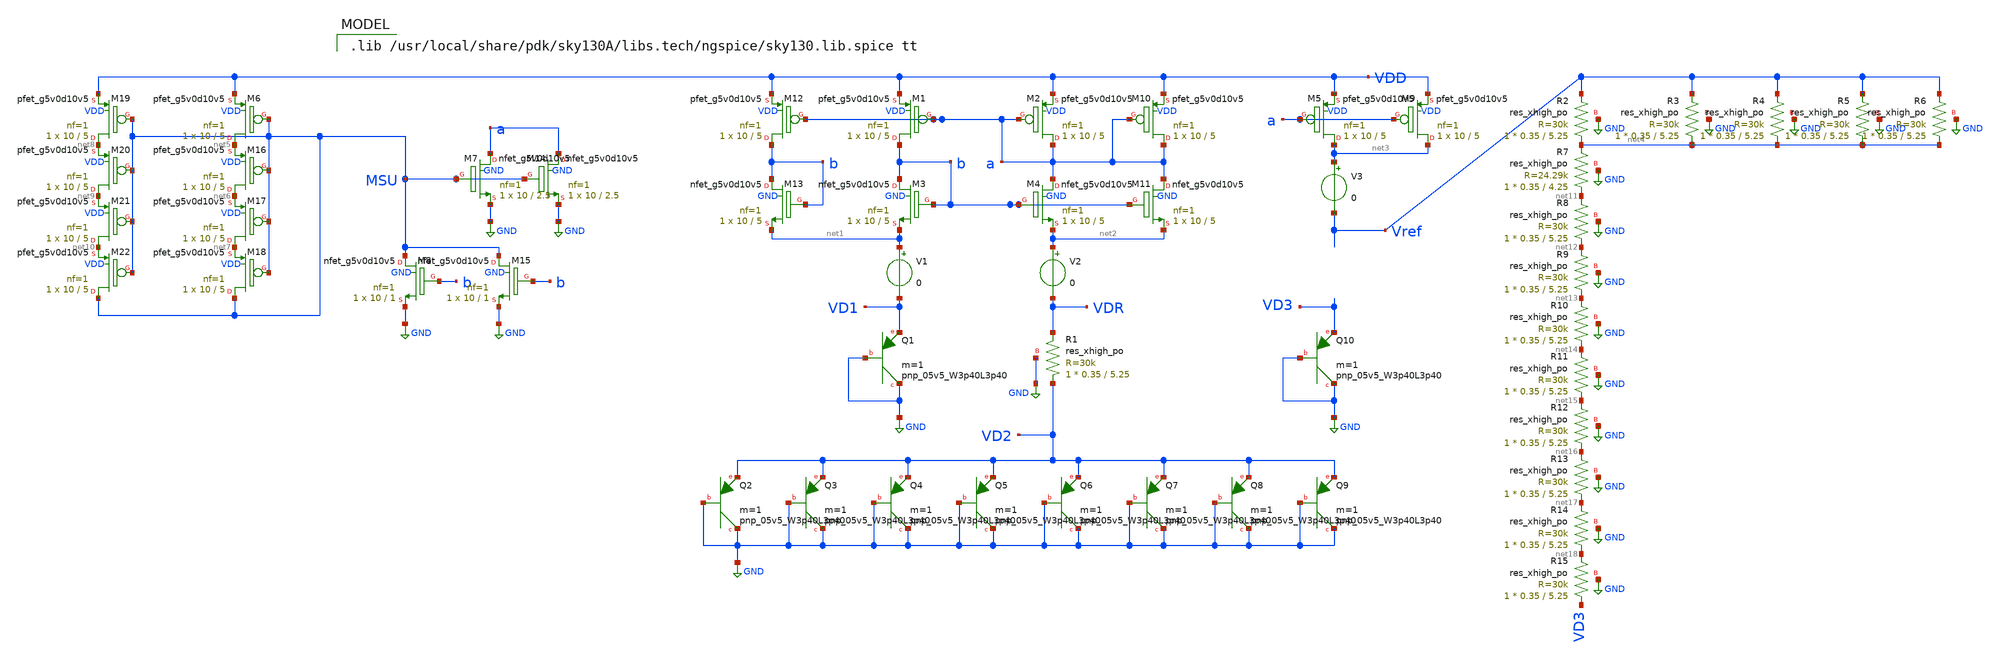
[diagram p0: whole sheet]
** sch_path: 2_BGR_nocas_30k_3p4pnp_finger.sch
**.subckt 2_BGR_nocas_30k_3p4pnp_finger
V1 net1 VD1 0
V2 net2 VDR 0
V3 net3 Vref 0
XM1 b a VDD VDD sky130_fd_pr__pfet_g5v0d10v5 L=5 W=10 nf=1 ad='int((nf+1)/2) * W/nf * 0.29' as='int((nf+2)/2) * W/nf * 0.29'
+ pd='2*int((nf+1)/2) * (W/nf + 0.29)' ps='2*int((nf+2)/2) * (W/nf + 0.29)' nrd='0.29 / W' nrs='0.29 / W'
+ sa=0 sb=0 sd=0 mult=1 m=1
XM2 a a VDD VDD sky130_fd_pr__pfet_g5v0d10v5 L=5 W=10 nf=1 ad='int((nf+1)/2) * W/nf * 0.29' as='int((nf+2)/2) * W/nf * 0.29'
+ pd='2*int((nf+1)/2) * (W/nf + 0.29)' ps='2*int((nf+2)/2) * (W/nf + 0.29)' nrd='0.29 / W' nrs='0.29 / W'
+ sa=0 sb=0 sd=0 mult=1 m=1
XM3 b b net1 GND sky130_fd_pr__nfet_g5v0d10v5 L=5 W=10 nf=1 ad='int((nf+1)/2) * W/nf * 0.29' as='int((nf+2)/2) * W/nf * 0.29'
+ pd='2*int((nf+1)/2) * (W/nf + 0.29)' ps='2*int((nf+2)/2) * (W/nf + 0.29)' nrd='0.29 / W' nrs='0.29 / W'
+ sa=0 sb=0 sd=0 mult=1 m=1
XM4 a b net2 GND sky130_fd_pr__nfet_g5v0d10v5 L=5 W=10 nf=1 ad='int((nf+1)/2) * W/nf * 0.29' as='int((nf+2)/2) * W/nf * 0.29'
+ pd='2*int((nf+1)/2) * (W/nf + 0.29)' ps='2*int((nf+2)/2) * (W/nf + 0.29)' nrd='0.29 / W' nrs='0.29 / W'
+ sa=0 sb=0 sd=0 mult=1 m=1
XM5 net3 a VDD VDD sky130_fd_pr__pfet_g5v0d10v5 L=5 W=10 nf=1 ad='int((nf+1)/2) * W/nf * 0.29' as='int((nf+2)/2) * W/nf * 0.29'
+ pd='2*int((nf+1)/2) * (W/nf + 0.29)' ps='2*int((nf+2)/2) * (W/nf + 0.29)' nrd='0.29 / W' nrs='0.29 / W'
+ sa=0 sb=0 sd=0 mult=1 m=1
XM8 MSU b GND GND sky130_fd_pr__nfet_g5v0d10v5 L=1 W=10 nf=1 ad='int((nf+1)/2) * W/nf * 0.29' as='int((nf+2)/2) * W/nf * 0.29'
+ pd='2*int((nf+1)/2) * (W/nf + 0.29)' ps='2*int((nf+2)/2) * (W/nf + 0.29)' nrd='0.29 / W' nrs='0.29 / W'
+ sa=0 sb=0 sd=0 mult=1 m=1
XM7 a MSU GND GND sky130_fd_pr__nfet_g5v0d10v5 L=2.5 W=10 nf=1 ad='int((nf+1)/2) * W/nf * 0.29' as='int((nf+2)/2) * W/nf * 0.29'
+ pd='2*int((nf+1)/2) * (W/nf + 0.29)' ps='2*int((nf+2)/2) * (W/nf + 0.29)' nrd='0.29 / W' nrs='0.29 / W'
+ sa=0 sb=0 sd=0 mult=1 m=1
XQ1 GND GND VD1 sky130_fd_pr__pnp_05v5_W3p40L3p40 m=1
XQ2 GND GND VD2 sky130_fd_pr__pnp_05v5_W3p40L3p40 m=1
XQ3 GND GND VD2 sky130_fd_pr__pnp_05v5_W3p40L3p40 m=1
XQ4 GND GND VD2 sky130_fd_pr__pnp_05v5_W3p40L3p40 m=1
XQ5 GND GND VD2 sky130_fd_pr__pnp_05v5_W3p40L3p40 m=1
XQ6 GND GND VD2 sky130_fd_pr__pnp_05v5_W3p40L3p40 m=1
XQ7 GND GND VD2 sky130_fd_pr__pnp_05v5_W3p40L3p40 m=1
XQ8 GND GND VD2 sky130_fd_pr__pnp_05v5_W3p40L3p40 m=1
XQ9 GND GND VD2 sky130_fd_pr__pnp_05v5_W3p40L3p40 m=1
XQ10 GND GND VD3 sky130_fd_pr__pnp_05v5_W3p40L3p40 m=1
XM6 net5 MSU VDD VDD sky130_fd_pr__pfet_g5v0d10v5 L=5 W=10 nf=1 ad='int((nf+1)/2) * W/nf * 0.29' as='int((nf+2)/2) * W/nf * 0.29'
+ pd='2*int((nf+1)/2) * (W/nf + 0.29)' ps='2*int((nf+2)/2) * (W/nf + 0.29)' nrd='0.29 / W' nrs='0.29 / W'
+ sa=0 sb=0 sd=0 mult=1 m=1
XM9 net3 a VDD VDD sky130_fd_pr__pfet_g5v0d10v5 L=5 W=10 nf=1 ad='int((nf+1)/2) * W/nf * 0.29' as='int((nf+2)/2) * W/nf * 0.29'
+ pd='2*int((nf+1)/2) * (W/nf + 0.29)' ps='2*int((nf+2)/2) * (W/nf + 0.29)' nrd='0.29 / W' nrs='0.29 / W'
+ sa=0 sb=0 sd=0 mult=1 m=1
XM10 a a VDD VDD sky130_fd_pr__pfet_g5v0d10v5 L=5 W=10 nf=1 ad='int((nf+1)/2) * W/nf * 0.29' as='int((nf+2)/2) * W/nf * 0.29'
+ pd='2*int((nf+1)/2) * (W/nf + 0.29)' ps='2*int((nf+2)/2) * (W/nf + 0.29)' nrd='0.29 / W' nrs='0.29 / W'
+ sa=0 sb=0 sd=0 mult=1 m=1
XM11 a b net2 GND sky130_fd_pr__nfet_g5v0d10v5 L=5 W=10 nf=1 ad='int((nf+1)/2) * W/nf * 0.29' as='int((nf+2)/2) * W/nf * 0.29'
+ pd='2*int((nf+1)/2) * (W/nf + 0.29)' ps='2*int((nf+2)/2) * (W/nf + 0.29)' nrd='0.29 / W' nrs='0.29 / W'
+ sa=0 sb=0 sd=0 mult=1 m=1
XM12 b a VDD VDD sky130_fd_pr__pfet_g5v0d10v5 L=5 W=10 nf=1 ad='int((nf+1)/2) * W/nf * 0.29' as='int((nf+2)/2) * W/nf * 0.29'
+ pd='2*int((nf+1)/2) * (W/nf + 0.29)' ps='2*int((nf+2)/2) * (W/nf + 0.29)' nrd='0.29 / W' nrs='0.29 / W'
+ sa=0 sb=0 sd=0 mult=1 m=1
XM13 b b net1 GND sky130_fd_pr__nfet_g5v0d10v5 L=5 W=10 nf=1 ad='int((nf+1)/2) * W/nf * 0.29' as='int((nf+2)/2) * W/nf * 0.29'
+ pd='2*int((nf+1)/2) * (W/nf + 0.29)' ps='2*int((nf+2)/2) * (W/nf + 0.29)' nrd='0.29 / W' nrs='0.29 / W'
+ sa=0 sb=0 sd=0 mult=1 m=1
XM14 a MSU GND GND sky130_fd_pr__nfet_g5v0d10v5 L=2.5 W=10 nf=1 ad='int((nf+1)/2) * W/nf * 0.29' as='int((nf+2)/2) * W/nf * 0.29'
+ pd='2*int((nf+1)/2) * (W/nf + 0.29)' ps='2*int((nf+2)/2) * (W/nf + 0.29)' nrd='0.29 / W' nrs='0.29 / W'
+ sa=0 sb=0 sd=0 mult=1 m=1
XM15 MSU b GND GND sky130_fd_pr__nfet_g5v0d10v5 L=1 W=10 nf=1 ad='int((nf+1)/2) * W/nf * 0.29' as='int((nf+2)/2) * W/nf * 0.29'
+ pd='2*int((nf+1)/2) * (W/nf + 0.29)' ps='2*int((nf+2)/2) * (W/nf + 0.29)' nrd='0.29 / W' nrs='0.29 / W'
+ sa=0 sb=0 sd=0 mult=1 m=1
XM16 net6 MSU net5 VDD sky130_fd_pr__pfet_g5v0d10v5 L=5 W=10 nf=1 ad='int((nf+1)/2) * W/nf * 0.29' as='int((nf+2)/2) * W/nf * 0.29'
+ pd='2*int((nf+1)/2) * (W/nf + 0.29)' ps='2*int((nf+2)/2) * (W/nf + 0.29)' nrd='0.29 / W' nrs='0.29 / W'
+ sa=0 sb=0 sd=0 mult=1 m=1
XM17 net7 MSU net6 VDD sky130_fd_pr__pfet_g5v0d10v5 L=5 W=10 nf=1 ad='int((nf+1)/2) * W/nf * 0.29' as='int((nf+2)/2) * W/nf * 0.29'
+ pd='2*int((nf+1)/2) * (W/nf + 0.29)' ps='2*int((nf+2)/2) * (W/nf + 0.29)' nrd='0.29 / W' nrs='0.29 / W'
+ sa=0 sb=0 sd=0 mult=1 m=1
XM18 MSU MSU net7 VDD sky130_fd_pr__pfet_g5v0d10v5 L=5 W=10 nf=1 ad='int((nf+1)/2) * W/nf * 0.29' as='int((nf+2)/2) * W/nf * 0.29'
+ pd='2*int((nf+1)/2) * (W/nf + 0.29)' ps='2*int((nf+2)/2) * (W/nf + 0.29)' nrd='0.29 / W' nrs='0.29 / W'
+ sa=0 sb=0 sd=0 mult=1 m=1
XM19 net8 MSU VDD VDD sky130_fd_pr__pfet_g5v0d10v5 L=5 W=10 nf=1 ad='int((nf+1)/2) * W/nf * 0.29' as='int((nf+2)/2) * W/nf * 0.29'
+ pd='2*int((nf+1)/2) * (W/nf + 0.29)' ps='2*int((nf+2)/2) * (W/nf + 0.29)' nrd='0.29 / W' nrs='0.29 / W'
+ sa=0 sb=0 sd=0 mult=1 m=1
XM20 net9 MSU net8 VDD sky130_fd_pr__pfet_g5v0d10v5 L=5 W=10 nf=1 ad='int((nf+1)/2) * W/nf * 0.29' as='int((nf+2)/2) * W/nf * 0.29'
+ pd='2*int((nf+1)/2) * (W/nf + 0.29)' ps='2*int((nf+2)/2) * (W/nf + 0.29)' nrd='0.29 / W' nrs='0.29 / W'
+ sa=0 sb=0 sd=0 mult=1 m=1
XM21 net10 MSU net9 VDD sky130_fd_pr__pfet_g5v0d10v5 L=5 W=10 nf=1 ad='int((nf+1)/2) * W/nf * 0.29' as='int((nf+2)/2) * W/nf * 0.29'
+ pd='2*int((nf+1)/2) * (W/nf + 0.29)' ps='2*int((nf+2)/2) * (W/nf + 0.29)' nrd='0.29 / W' nrs='0.29 / W'
+ sa=0 sb=0 sd=0 mult=1 m=1
XM22 MSU MSU net10 VDD sky130_fd_pr__pfet_g5v0d10v5 L=5 W=10 nf=1 ad='int((nf+1)/2) * W/nf * 0.29' as='int((nf+2)/2) * W/nf * 0.29'
+ pd='2*int((nf+1)/2) * (W/nf + 0.29)' ps='2*int((nf+2)/2) * (W/nf + 0.29)' nrd='0.29 / W' nrs='0.29 / W'
+ sa=0 sb=0 sd=0 mult=1 m=1
XR1 VD2 VDR GND sky130_fd_pr__res_xhigh_po W=0.35 L=5.25 mult=1 m=1
XR2 net4 Vref GND sky130_fd_pr__res_xhigh_po W=0.35 L=5.25 mult=1 m=1
XR3 net4 Vref GND sky130_fd_pr__res_xhigh_po W=0.35 L=5.25 mult=1 m=1
XR4 net4 Vref GND sky130_fd_pr__res_xhigh_po W=0.35 L=5.25 mult=1 m=1
XR5 net4 Vref GND sky130_fd_pr__res_xhigh_po W=0.35 L=5.25 mult=1 m=1
XR6 net4 Vref GND sky130_fd_pr__res_xhigh_po W=0.35 L=5.25 mult=1 m=1
XR7 net11 net4 GND sky130_fd_pr__res_xhigh_po W=0.35 L=4.25 mult=1 m=1
XR8 net12 net11 GND sky130_fd_pr__res_xhigh_po W=0.35 L=5.25 mult=1 m=1
XR9 net13 net12 GND sky130_fd_pr__res_xhigh_po W=0.35 L=5.25 mult=1 m=1
XR10 net14 net13 GND sky130_fd_pr__res_xhigh_po W=0.35 L=5.25 mult=1 m=1
XR11 net15 net14 GND sky130_fd_pr__res_xhigh_po W=0.35 L=5.25 mult=1 m=1
XR12 net16 net15 GND sky130_fd_pr__res_xhigh_po W=0.35 L=5.25 mult=1 m=1
XR13 net17 net16 GND sky130_fd_pr__res_xhigh_po W=0.35 L=5.25 mult=1 m=1
XR14 net18 net17 GND sky130_fd_pr__res_xhigh_po W=0.35 L=5.25 mult=1 m=1
XR15 VD3 net18 GND sky130_fd_pr__res_xhigh_po W=0.35 L=5.25 mult=1 m=1
**** begin user architecture code

.lib /usr/local/share/pdk/sky130A/libs.tech/ngspice/sky130.lib.spice tt


.save all
Vdd Vdd 0 DC 0 AC 0
*** Plot color settings***
.control
set color0=white  color1=black color2=blue color3=red
set color4=magenta  color5=cyan  xbrushwidth=3
.endc
*** Temp variation ***
.control
alter Vdd DC=3.3
dc temp -40 125 0.1
plot V1#branch V2#branch V3#branch
plot Vref
plot (deriv(Vref)/Vref)
.endc
************************
*** Supply variation ***
.control
dc Vdd 1.5 5.5 1m
plot Vref
.endc
************************
*** PSRR analysis ***
.control
alter Vdd DC=3.3
alter Vdd AC=1
ac dec 10 1 10G
plot db(Vref)
.endc
*************************
*** Transient analysis ***
.control
alter @Vdd[pwl]=[ 0 0 100u 0 200u 3.3 500u 3.3 ]
tran 100u 500u
plot Vdd Vref
.endc
*************************
.end

**** end user architecture code
**.ends
.GLOBAL GND
.end
